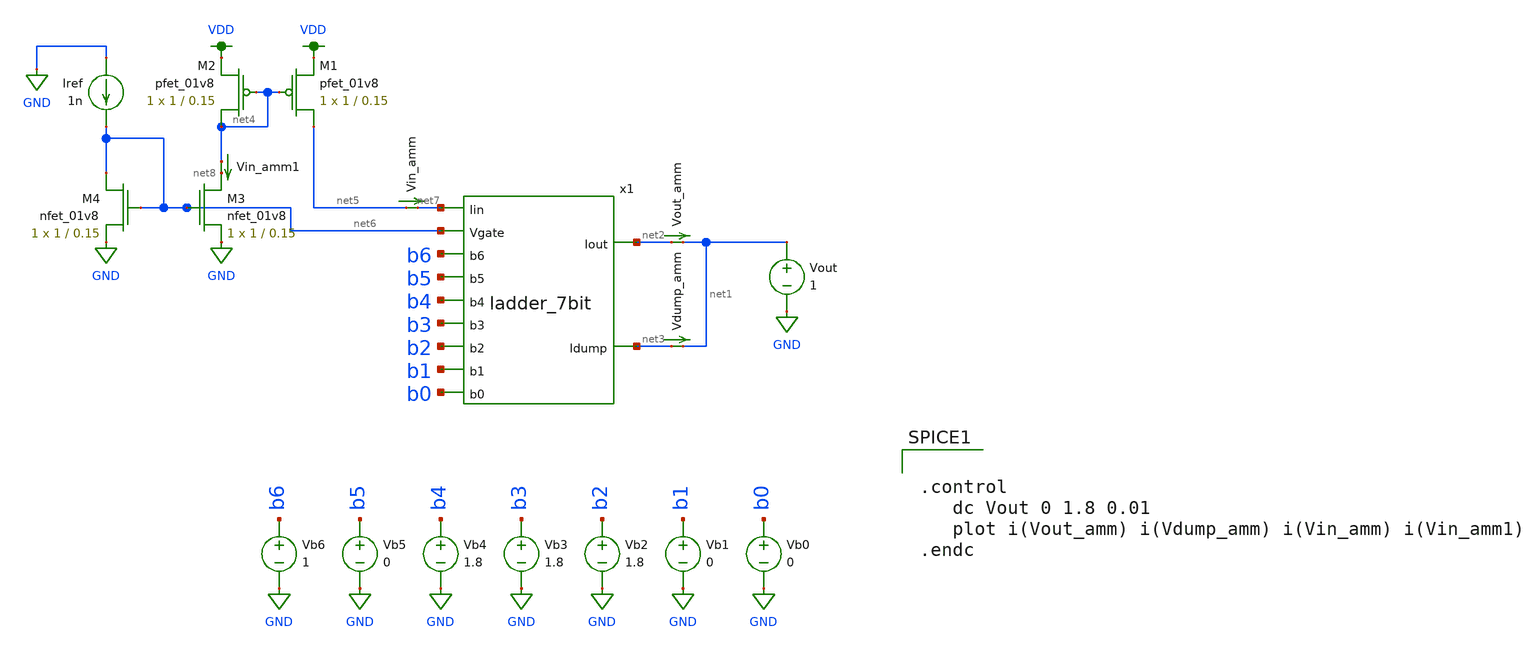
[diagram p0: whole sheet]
** sch_path: test_harness_dcvout.sch
**.subckt test_harness_dcvout
Vb0 b0 GND 0
Vb1 b1 GND 0
Vb2 b2 GND 1.8
Vb3 b3 GND 1.8
Vb4 b4 GND 1.8
Vb5 b5 GND 0
Vb6 b6 GND 1
Vout net1 GND 1
Vout_amm net2 net1 0
.save i(vout_amm)
Vdump_amm net3 net1 0
.save i(vdump_amm)
Iref GND net6 1n
XM1 net5 net4 VDD VDD sky130_fd_pr__pfet_01v8 L=0.15 W=1 nf=1 ad='int((nf+1)/2) * W/nf * 0.29' as='int((nf+2)/2) * W/nf * 0.29'
+ pd='2*int((nf+1)/2) * (W/nf + 0.29)' ps='2*int((nf+2)/2) * (W/nf + 0.29)' nrd='0.29 / W' nrs='0.29 / W'
+ sa=0 sb=0 sd=0 mult=1 m=1
XM2 net4 net4 VDD VDD sky130_fd_pr__pfet_01v8 L=0.15 W=1 nf=1 ad='int((nf+1)/2) * W/nf * 0.29' as='int((nf+2)/2) * W/nf * 0.29'
+ pd='2*int((nf+1)/2) * (W/nf + 0.29)' ps='2*int((nf+2)/2) * (W/nf + 0.29)' nrd='0.29 / W' nrs='0.29 / W'
+ sa=0 sb=0 sd=0 mult=1 m=1
XM3 net8 net6 GND GND sky130_fd_pr__nfet_01v8 L=0.15 W=1 nf=1 ad='int((nf+1)/2) * W/nf * 0.29' as='int((nf+2)/2) * W/nf * 0.29'
+ pd='2*int((nf+1)/2) * (W/nf + 0.29)' ps='2*int((nf+2)/2) * (W/nf + 0.29)' nrd='0.29 / W' nrs='0.29 / W'
+ sa=0 sb=0 sd=0 mult=1 m=1
x1 net6 net7 net3 net2 b5 b4 b1 b2 b3 b0 b6 ladder_7bit
XM4 net6 net6 GND GND sky130_fd_pr__nfet_01v8 L=0.15 W=1 nf=1 ad='int((nf+1)/2) * W/nf * 0.29' as='int((nf+2)/2) * W/nf * 0.29'
+ pd='2*int((nf+1)/2) * (W/nf + 0.29)' ps='2*int((nf+2)/2) * (W/nf + 0.29)' nrd='0.29 / W' nrs='0.29 / W'
+ sa=0 sb=0 sd=0 mult=1 m=1
Vin_amm net5 net7 0
.save i(vin_amm)
Vin_amm1 net4 net8 0
.save i(vin_amm1)
**** begin user architecture code


.control
   dc Vout 0 1.8 0.01
   plot i(Vout_amm) i(Vdump_amm) i(Vin_amm) i(Vin_amm1)
.endc


.option wnflag=1
.param MC_SWITCH=0.0
.lib ~/skywater/skywater-pdk/libraries/sky130_fd_pr_ngspice/latest/models/sky130.lib.spice tt

**** end user architecture code
**.ends

* expanding   symbol:  ./ladder_7bit.sym # of pins=11
** sym_path: ladder_7bit.sym
** sch_path: ladder_7bit.sch
.subckt ladder_7bit Vgate Iin Idump Iout b5 b4 b1 b2 b3 b0 b6
*.opin Idump
*.opin Iout
*.ipin Vgate
*.ipin Iin
*.ipin b6
*.ipin b5
*.ipin b4
*.ipin b3
*.ipin b2
*.ipin b1
*.ipin b0
x1 Iin net8 Vgate Idump Iout net1 b6 ladder_1bit
x2 net8 net9 Vgate Idump Iout net2 b5 ladder_1bit
x3 net9 net10 Vgate Idump Iout net3 b4 ladder_1bit
x4 net10 net11 Vgate Idump Iout net4 b3 ladder_1bit
x5 net11 net12 Vgate Idump Iout net5 b2 ladder_1bit
x6 net12 net13 Vgate Idump Iout net6 b1 ladder_1bit
x7 net13 net14 Vgate Idump Iout net7 b0 ladder_1bit
XM1 Idump Vgate net14 GND sky130_fd_pr__nfet_01v8 L=0.15 W=1 nf=1 ad='int((nf+1)/2) * W/nf * 0.29' as='int((nf+2)/2) * W/nf * 0.29'
+ pd='2*int((nf+1)/2) * (W/nf + 0.29)' ps='2*int((nf+2)/2) * (W/nf + 0.29)' nrd='0.29 / W' nrs='0.29 / W'
+ sa=0 sb=0 sd=0 mult=1 m=1
X8 b6 net15 VDD GND inverter
X9 b5 net16 VDD GND inverter
X10 b4 net17 VDD GND inverter
X11 b3 net18 VDD GND inverter
X12 b2 net19 VDD GND inverter
X13 b1 net20 VDD GND inverter
X14 b0 net21 VDD GND inverter
.ends


* expanding   symbol:  /home/madvlsi/R2R-DAC/ladder_1bit.sym # of pins=7
** sym_path: ladder_1bit.sym
** sch_path: ladder_1bit.sch
.subckt ladder_1bit Iin_in Iin_out Vg I_dump Iout B_bar B
*.ipin Iin_in
*.ipin Vg
*.ipin B
*.ipin B_bar
*.opin Iin_out
*.opin I_dump
*.opin Iout
XM5 net1 Vg Iin_in GND sky130_fd_pr__nfet_01v8 L=0.15 W=1 nf=1 ad='int((nf+1)/2) * W/nf * 0.29' as='int((nf+2)/2) * W/nf * 0.29'
+ pd='2*int((nf+1)/2) * (W/nf + 0.29)' ps='2*int((nf+2)/2) * (W/nf + 0.29)' nrd='0.29 / W' nrs='0.29 / W'
+ sa=0 sb=0 sd=0 mult=1 m=1
XM6 Iout B net1 GND sky130_fd_pr__nfet_01v8 L=0.15 W=1 nf=1 ad='int((nf+1)/2) * W/nf * 0.29' as='int((nf+2)/2) * W/nf * 0.29'
+ pd='2*int((nf+1)/2) * (W/nf + 0.29)' ps='2*int((nf+2)/2) * (W/nf + 0.29)' nrd='0.29 / W' nrs='0.29 / W'
+ sa=0 sb=0 sd=0 mult=1 m=1
XM7 net1 B_bar I_dump GND sky130_fd_pr__nfet_01v8 L=0.15 W=1 nf=1 ad='int((nf+1)/2) * W/nf * 0.29' as='int((nf+2)/2) * W/nf * 0.29'
+ pd='2*int((nf+1)/2) * (W/nf + 0.29)' ps='2*int((nf+2)/2) * (W/nf + 0.29)' nrd='0.29 / W' nrs='0.29 / W'
+ sa=0 sb=0 sd=0 mult=1 m=1
XM8 Iin_in Vg Iin_out GND sky130_fd_pr__nfet_01v8 L=0.15 W=1 nf=1 ad='int((nf+1)/2) * W/nf * 0.29' as='int((nf+2)/2) * W/nf * 0.29'
+ pd='2*int((nf+1)/2) * (W/nf + 0.29)' ps='2*int((nf+2)/2) * (W/nf + 0.29)' nrd='0.29 / W' nrs='0.29 / W'
+ sa=0 sb=0 sd=0 mult=1 m=1
.ends


* expanding   symbol:  /home/madvlsi/Documents/mp1/inverter.sym # of pins=4
** sym_path: /home/madvlsi/Documents/mp1/inverter.sym
** sch_path: /home/madvlsi/Documents/mp1/inverter.sch
.subckt inverter A Y VP VN
*.ipin A
*.iopin VP
*.iopin VN
*.opin Y
XM3 Y A VP VP sky130_fd_pr__pfet_01v8 L=0.15 W=1 nf=1 ad='int((nf+1)/2) * W/nf * 0.29' as='int((nf+2)/2) * W/nf * 0.29'
+ pd='2*int((nf+1)/2) * (W/nf + 0.29)' ps='2*int((nf+2)/2) * (W/nf + 0.29)' nrd='0.29 / W' nrs='0.29 / W'
+ sa=0 sb=0 sd=0 mult=1 m=1
XM4 Y A VN VN sky130_fd_pr__nfet_01v8 L=0.15 W=1 nf=1 ad='int((nf+1)/2) * W/nf * 0.29' as='int((nf+2)/2) * W/nf * 0.29'
+ pd='2*int((nf+1)/2) * (W/nf + 0.29)' ps='2*int((nf+2)/2) * (W/nf + 0.29)' nrd='0.29 / W' nrs='0.29 / W'
+ sa=0 sb=0 sd=0 mult=1 m=1
.ends

.GLOBAL GND
.GLOBAL VDD
.end
